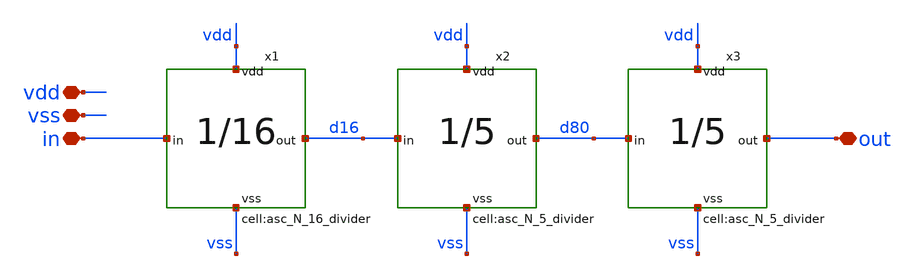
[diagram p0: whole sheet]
** sch_path: designs/libs/xp_core_analog/asc_program_counter_400/asc_program_counter_400.sch
**.subckt asc_program_counter_400 vdd vss in out
*.iopin vdd
*.iopin vss
*.iopin in
*.iopin out
x1 in d16 vdd vss asc_N_16_divider
x2 d16 d80 vdd vss asc_N_5_divider
x3 d80 out vdd vss asc_N_5_divider
**.ends
.end
